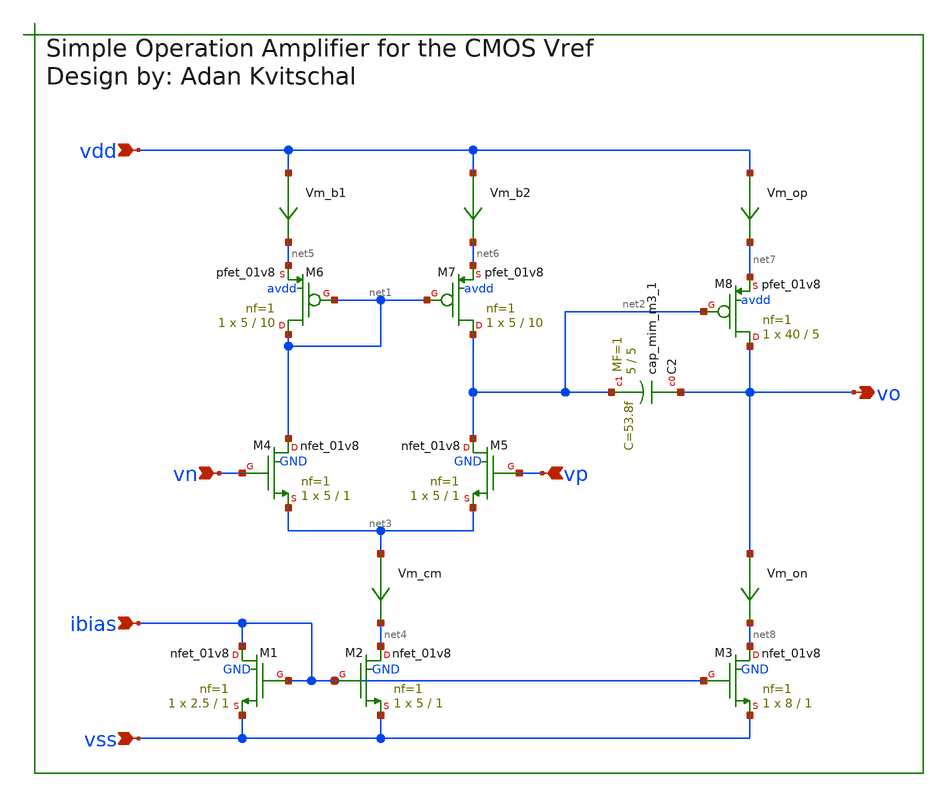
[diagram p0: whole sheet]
** sch_path: xschem/output_amp.sch
**.subckt output_amp vp vn ibias vo vss vdd
*.ipin vp
*.ipin vn
*.ipin ibias
*.opin vo
*.ipin vss
*.ipin vdd
XM1 ibias ibias vss GND sky130_fd_pr__nfet_01v8 L=1 W=2.5 nf=1 ad='int((nf+1)/2) * W/nf * 0.29' as='int((nf+2)/2) * W/nf * 0.29'
+ pd='2*int((nf+1)/2) * (W/nf + 0.29)' ps='2*int((nf+2)/2) * (W/nf + 0.29)' nrd='0.29 / W' nrs='0.29 / W'
+ sa=0 sb=0 sd=0 mult=1 m=1
XM2 net4 ibias vss GND sky130_fd_pr__nfet_01v8 L=1 W=5 nf=1 ad='int((nf+1)/2) * W/nf * 0.29' as='int((nf+2)/2) * W/nf * 0.29'
+ pd='2*int((nf+1)/2) * (W/nf + 0.29)' ps='2*int((nf+2)/2) * (W/nf + 0.29)' nrd='0.29 / W' nrs='0.29 / W'
+ sa=0 sb=0 sd=0 mult=1 m=1
XM7 net2 net1 net6 avdd sky130_fd_pr__pfet_01v8 L=10 W=5 nf=1 ad='int((nf+1)/2) * W/nf * 0.29' as='int((nf+2)/2) * W/nf * 0.29'
+ pd='2*int((nf+1)/2) * (W/nf + 0.29)' ps='2*int((nf+2)/2) * (W/nf + 0.29)' nrd='0.29 / W' nrs='0.29 / W'
+ sa=0 sb=0 sd=0 mult=1 m=1
XM4 net1 vn net3 GND sky130_fd_pr__nfet_01v8 L=1 W=5 nf=1 ad='int((nf+1)/2) * W/nf * 0.29' as='int((nf+2)/2) * W/nf * 0.29'
+ pd='2*int((nf+1)/2) * (W/nf + 0.29)' ps='2*int((nf+2)/2) * (W/nf + 0.29)' nrd='0.29 / W' nrs='0.29 / W'
+ sa=0 sb=0 sd=0 mult=1 m=1
XM5 net2 vp net3 GND sky130_fd_pr__nfet_01v8 L=1 W=5 nf=1 ad='int((nf+1)/2) * W/nf * 0.29' as='int((nf+2)/2) * W/nf * 0.29'
+ pd='2*int((nf+1)/2) * (W/nf + 0.29)' ps='2*int((nf+2)/2) * (W/nf + 0.29)' nrd='0.29 / W' nrs='0.29 / W'
+ sa=0 sb=0 sd=0 mult=1 m=1
XM6 net1 net1 net5 avdd sky130_fd_pr__pfet_01v8 L=10 W=5 nf=1 ad='int((nf+1)/2) * W/nf * 0.29' as='int((nf+2)/2) * W/nf * 0.29'
+ pd='2*int((nf+1)/2) * (W/nf + 0.29)' ps='2*int((nf+2)/2) * (W/nf + 0.29)' nrd='0.29 / W' nrs='0.29 / W'
+ sa=0 sb=0 sd=0 mult=1 m=1
Vm_b1 vdd net5 0
.save i(vm_b1)
XM3 net8 ibias vss GND sky130_fd_pr__nfet_01v8 L=1 W=8 nf=1 ad='int((nf+1)/2) * W/nf * 0.29' as='int((nf+2)/2) * W/nf * 0.29'
+ pd='2*int((nf+1)/2) * (W/nf + 0.29)' ps='2*int((nf+2)/2) * (W/nf + 0.29)' nrd='0.29 / W' nrs='0.29 / W'
+ sa=0 sb=0 sd=0 mult=1 m=1
XM8 vo net2 net7 avdd sky130_fd_pr__pfet_01v8 L=5 W=40 nf=1 ad='int((nf+1)/2) * W/nf * 0.29' as='int((nf+2)/2) * W/nf * 0.29'
+ pd='2*int((nf+1)/2) * (W/nf + 0.29)' ps='2*int((nf+2)/2) * (W/nf + 0.29)' nrd='0.29 / W' nrs='0.29 / W'
+ sa=0 sb=0 sd=0 mult=1 m=1
Vm_op vdd net7 0
.save i(vm_op)
Vm_cm net3 net4 0
.save i(vm_cm)
Vm_b2 vdd net6 0
.save i(vm_b2)
XC2 vo net2 sky130_fd_pr__cap_mim_m3_1 W=5 L=5 MF=1 m=1
Vm_on vo net8 0
.save i(vm_on)
**.ends
.end
